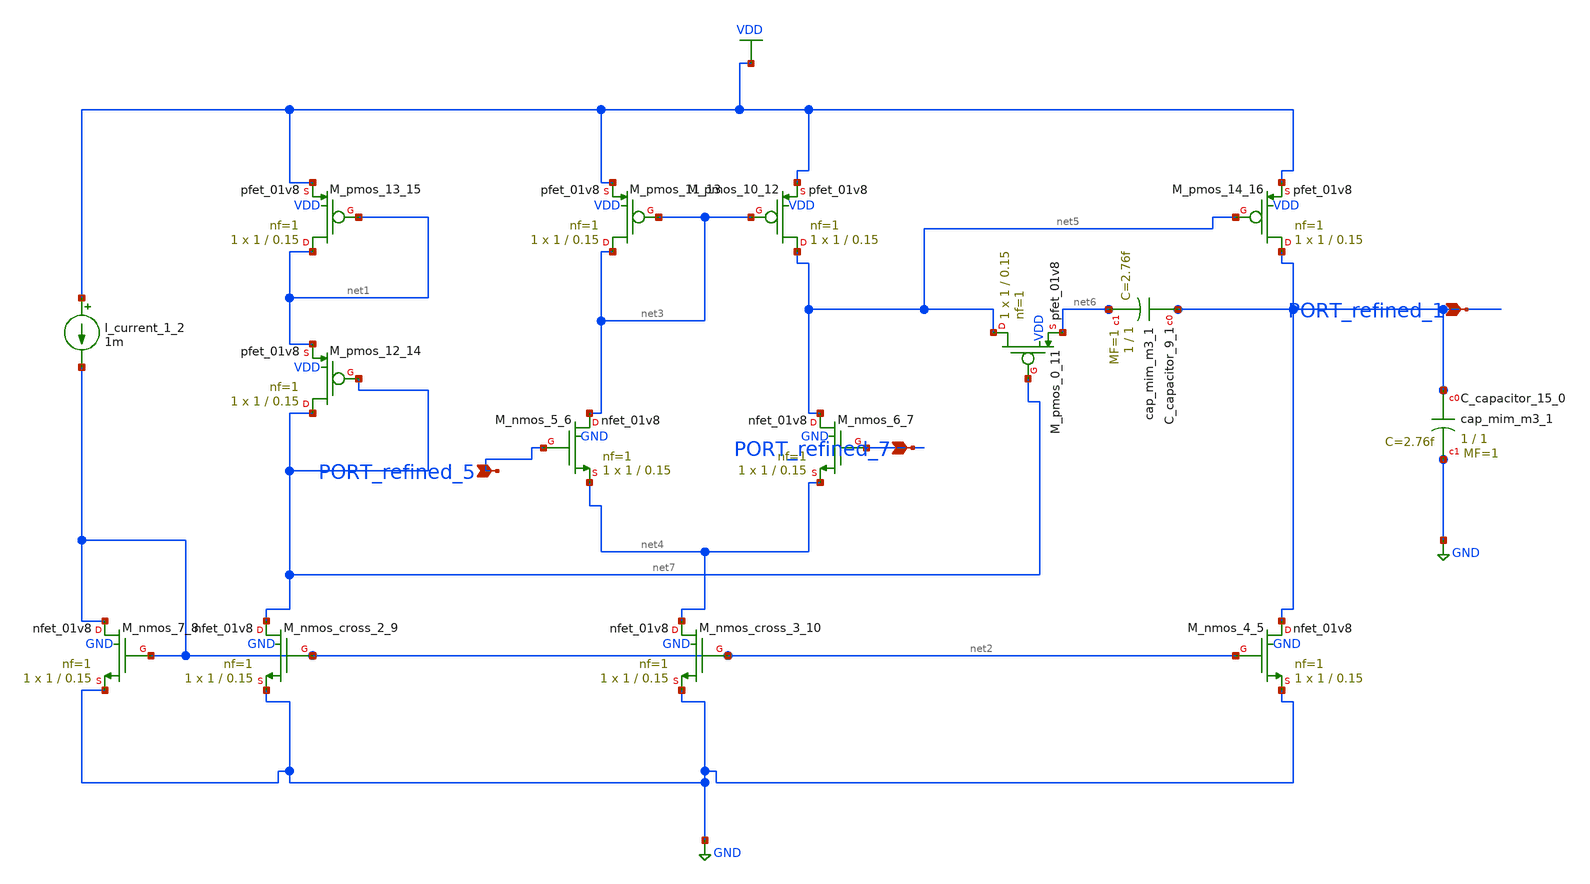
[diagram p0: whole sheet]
** sch_path: schematics/Image2Net/113.sch
**.subckt 113 PORT_refined_7 PORT_refined_5 PORT_refined_1
*.ipin PORT_refined_7
*.ipin PORT_refined_5
*.ipin PORT_refined_1
XC_capacitor_15_0 PORT_refined_1 GND sky130_fd_pr__cap_mim_m3_1 W=1 L=1 MF=1 m=1
XC_capacitor_9_1 PORT_refined_1 net6 sky130_fd_pr__cap_mim_m3_1 W=1 L=1 MF=1 m=1
I_current_1_2 VDD net2 1m
XM_nmos_4_5 PORT_refined_1 net2 GND GND sky130_fd_pr__nfet_01v8 L=0.15 W=1 nf=1 ad='int((1 + 1)/2) * 1 / 1 * 0.29'
+ as='int((1 + 2)/2) * 1 / 1 * 0.29' pd='2*int((1 + 1)/2) * (1 / 1 + 0.29)' ps='2*int((1 + 2)/2) * (1 / 1 + 0.29)'
+ nrd='0.29 / 1 ' nrs='0.29 / 1 ' sa=0 sb=0 sd=0 mult=1 m=1
XM_nmos_5_6 net3 PORT_refined_5 net4 GND sky130_fd_pr__nfet_01v8 L=0.15 W=1 nf=1 ad='int((1 + 1)/2) * 1 / 1 * 0.29'
+ as='int((1 + 2)/2) * 1 / 1 * 0.29' pd='2*int((1 + 1)/2) * (1 / 1 + 0.29)' ps='2*int((1 + 2)/2) * (1 / 1 + 0.29)'
+ nrd='0.29 / 1 ' nrs='0.29 / 1 ' sa=0 sb=0 sd=0 mult=1 m=1
XM_nmos_6_7 net5 PORT_refined_7 net4 GND sky130_fd_pr__nfet_01v8 L=0.15 W=1 nf=1 ad='int((1 + 1)/2) * 1 / 1 * 0.29'
+ as='int((1 + 2)/2) * 1 / 1 * 0.29' pd='2*int((1 + 1)/2) * (1 / 1 + 0.29)' ps='2*int((1 + 2)/2) * (1 / 1 + 0.29)'
+ nrd='0.29 / 1 ' nrs='0.29 / 1 ' sa=0 sb=0 sd=0 mult=1 m=1
XM_nmos_7_8 net2 net2 GND GND sky130_fd_pr__nfet_01v8 L=0.15 W=1 nf=1 ad='int((1 + 1)/2) * 1 / 1 * 0.29'
+ as='int((1 + 2)/2) * 1 / 1 * 0.29' pd='2*int((1 + 1)/2) * (1 / 1 + 0.29)' ps='2*int((1 + 2)/2) * (1 / 1 + 0.29)'
+ nrd='0.29 / 1 ' nrs='0.29 / 1 ' sa=0 sb=0 sd=0 mult=1 m=1
XM_nmos_cross_2_9 net7 net2 GND GND sky130_fd_pr__nfet_01v8 L=0.15 W=1 nf=1 ad='int((1 + 1)/2) * 1 / 1 * 0.29'
+ as='int((1 + 2)/2) * 1 / 1 * 0.29' pd='2*int((1 + 1)/2) * (1 / 1 + 0.29)' ps='2*int((1 + 2)/2) * (1 / 1 + 0.29)'
+ nrd='0.29 / 1 ' nrs='0.29 / 1 ' sa=0 sb=0 sd=0 mult=1 m=1
XM_nmos_cross_3_10 net4 net2 GND GND sky130_fd_pr__nfet_01v8 L=0.15 W=1 nf=1 ad='int((1 + 1)/2) * 1 / 1 * 0.29'
+ as='int((1 + 2)/2) * 1 / 1 * 0.29' pd='2*int((1 + 1)/2) * (1 / 1 + 0.29)' ps='2*int((1 + 2)/2) * (1 / 1 + 0.29)'
+ nrd='0.29 / 1 ' nrs='0.29 / 1 ' sa=0 sb=0 sd=0 mult=1 m=1
XM_pmos_0_11 net5 net7 net6 VDD sky130_fd_pr__pfet_01v8 L=0.15 W=1 nf=1 ad='int((1 + 1)/2) * 1 / 1 * 0.29'
+ as='int((1 + 2)/2) * 1 / 1 * 0.29' pd='2*int((1 + 1)/2) * (1 / 1 + 0.29)' ps='2*int((1 + 2)/2) * (1 / 1 + 0.29)'
+ nrd='0.29 / 1 ' nrs='0.29 / 1 ' sa=0 sb=0 sd=0 mult=1 m=1
XM_pmos_10_12 net5 net3 VDD VDD sky130_fd_pr__pfet_01v8 L=0.15 W=1 nf=1 ad='int((1 + 1)/2) * 1 / 1 * 0.29'
+ as='int((1 + 2)/2) * 1 / 1 * 0.29' pd='2*int((1 + 1)/2) * (1 / 1 + 0.29)' ps='2*int((1 + 2)/2) * (1 / 1 + 0.29)'
+ nrd='0.29 / 1 ' nrs='0.29 / 1 ' sa=0 sb=0 sd=0 mult=1 m=1
XM_pmos_11_13 net3 net3 VDD VDD sky130_fd_pr__pfet_01v8 L=0.15 W=1 nf=1 ad='int((1 + 1)/2) * 1 / 1 * 0.29'
+ as='int((1 + 2)/2) * 1 / 1 * 0.29' pd='2*int((1 + 1)/2) * (1 / 1 + 0.29)' ps='2*int((1 + 2)/2) * (1 / 1 + 0.29)'
+ nrd='0.29 / 1 ' nrs='0.29 / 1 ' sa=0 sb=0 sd=0 mult=1 m=1
XM_pmos_12_14 net7 net7 net1 VDD sky130_fd_pr__pfet_01v8 L=0.15 W=1 nf=1 ad='int((1 + 1)/2) * 1 / 1 * 0.29'
+ as='int((1 + 2)/2) * 1 / 1 * 0.29' pd='2*int((1 + 1)/2) * (1 / 1 + 0.29)' ps='2*int((1 + 2)/2) * (1 / 1 + 0.29)'
+ nrd='0.29 / 1 ' nrs='0.29 / 1 ' sa=0 sb=0 sd=0 mult=1 m=1
XM_pmos_13_15 net1 net1 VDD VDD sky130_fd_pr__pfet_01v8 L=0.15 W=1 nf=1 ad='int((1 + 1)/2) * 1 / 1 * 0.29'
+ as='int((1 + 2)/2) * 1 / 1 * 0.29' pd='2*int((1 + 1)/2) * (1 / 1 + 0.29)' ps='2*int((1 + 2)/2) * (1 / 1 + 0.29)'
+ nrd='0.29 / 1 ' nrs='0.29 / 1 ' sa=0 sb=0 sd=0 mult=1 m=1
XM_pmos_14_16 PORT_refined_1 net5 VDD VDD sky130_fd_pr__pfet_01v8 L=0.15 W=1 nf=1 ad='int((1 + 1)/2) * 1 / 1 * 0.29'
+ as='int((1 + 2)/2) * 1 / 1 * 0.29' pd='2*int((1 + 1)/2) * (1 / 1 + 0.29)' ps='2*int((1 + 2)/2) * (1 / 1 + 0.29)'
+ nrd='0.29 / 1 ' nrs='0.29 / 1 ' sa=0 sb=0 sd=0 mult=1 m=1
**.ends
.GLOBAL GND
.GLOBAL VDD
.end
